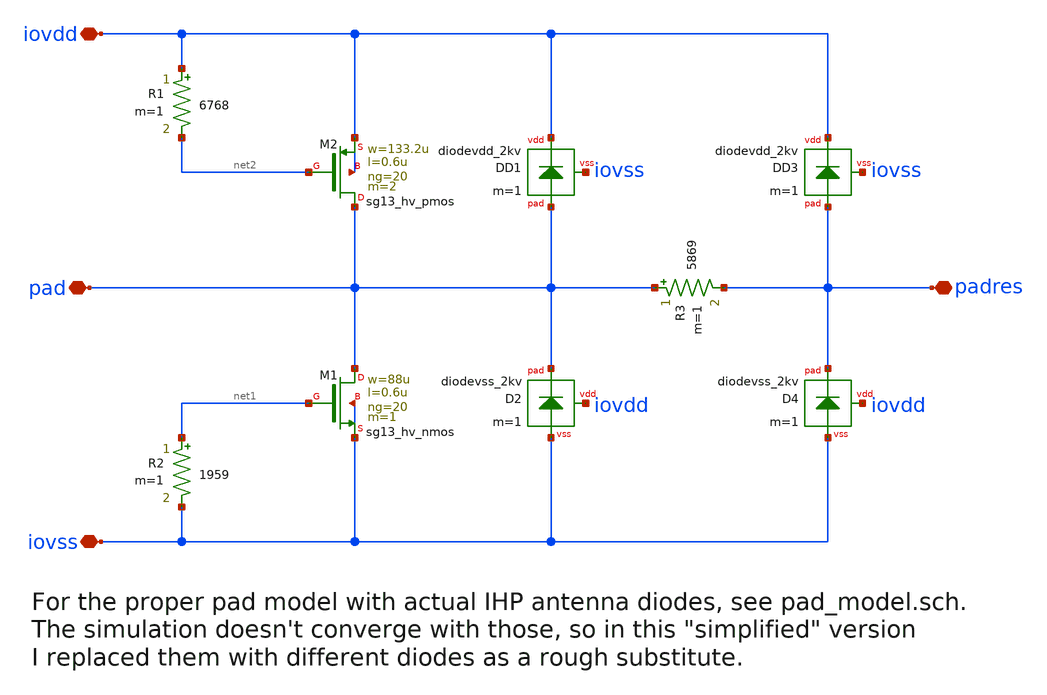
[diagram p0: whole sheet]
** sch_path: xschem/pad_model_simp.sch
**.subckt pad_model_simp pad padres iovdd iovss
*.iopin pad
*.iopin padres
*.iopin iovdd
*.iopin iovss
XM2 pad net2 iovdd iovdd sg13_hv_pmos w=133.2u l=0.6u ng=20 m=2 mm_ok=1
XM1 pad net1 iovss iovss sg13_hv_nmos w=88u l=0.6u ng=20 m=1 mm_ok=1
R1 iovdd net2 6768 m=1
R2 net1 iovss 1959 m=1
R3 pad padres 5869 m=1
XD1 iovdd pad iovss diodevdd_2kv m=1
XD2 iovdd pad iovss diodevss_2kv m=1
XD3 iovdd padres iovss diodevdd_2kv m=1
XD4 iovdd padres iovss diodevss_2kv m=1
**.ends
.end
